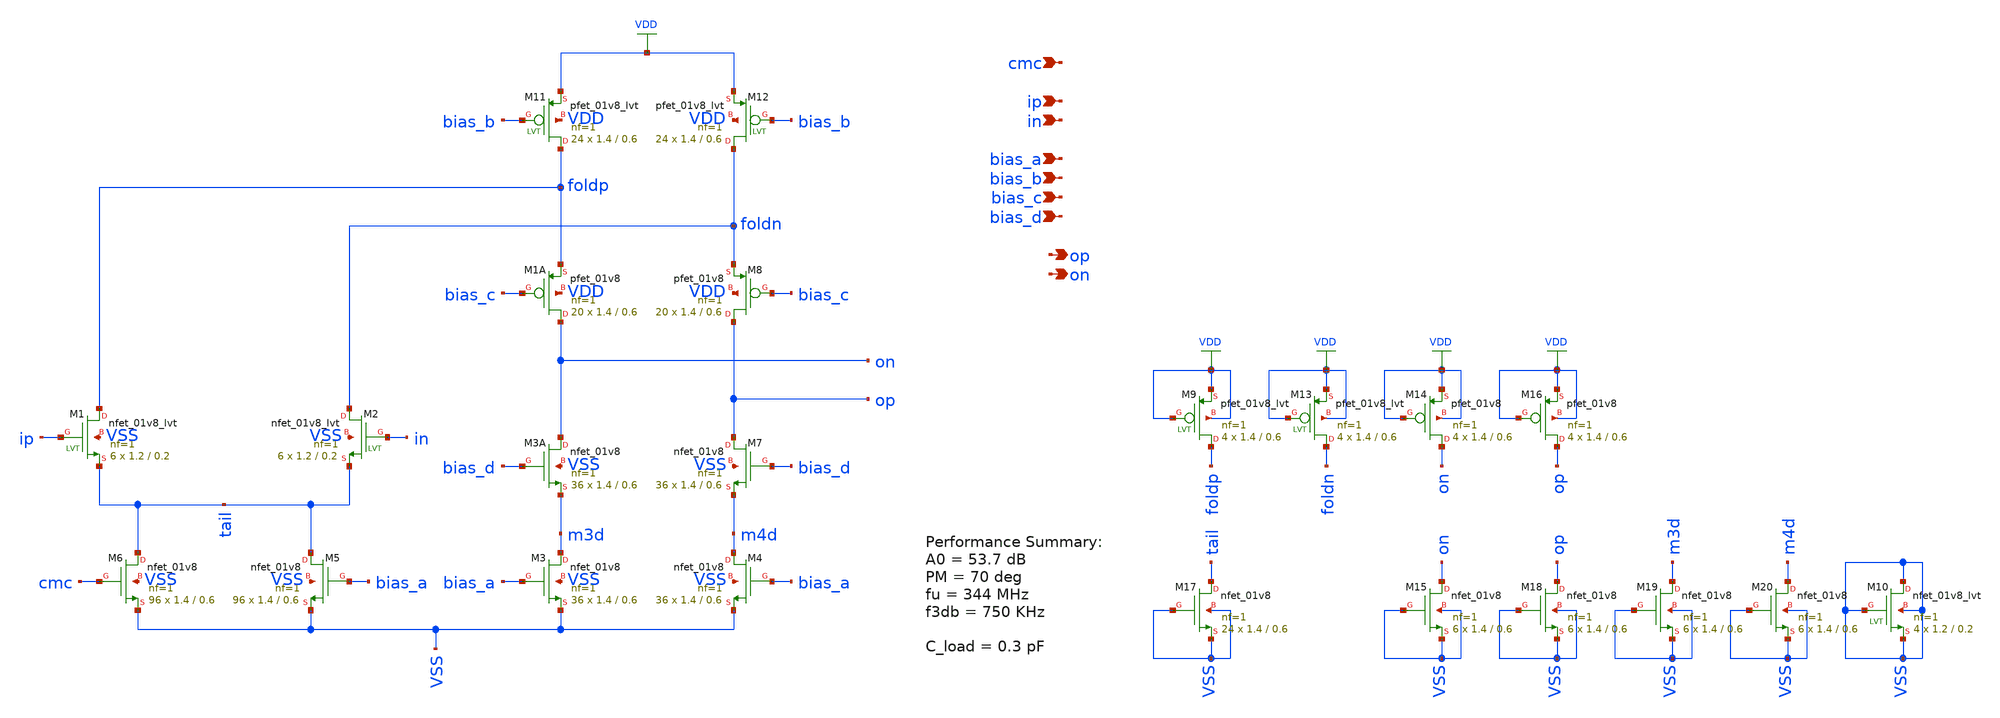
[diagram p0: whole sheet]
** sch_path: design/analog_modulator/schematic/folded_cascode_3_core.sch
**.subckt folded_cascode_3_core cmc ip in bias_a bias_b bias_c bias_d op on
*.ipin cmc
*.ipin ip
*.ipin in
*.ipin bias_a
*.ipin bias_b
*.ipin bias_c
*.ipin bias_d
*.opin op
*.opin on
XM1 foldp ip tail VSS sky130_fd_pr__nfet_01v8_lvt L=0.2 W=1.2 nf=1 ad='int((nf+1)/2) * W/nf * 0.29' as='int((nf+2)/2) * W/nf * 0.29'
+ pd='2*int((nf+1)/2) * (W/nf + 0.29)' ps='2*int((nf+2)/2) * (W/nf + 0.29)' nrd='0.29 / W' nrs='0.29 / W'
+ sa=0 sb=0 sd=0 mult=6 m=6
XM2 foldn in tail VSS sky130_fd_pr__nfet_01v8_lvt L=0.2 W=1.2 nf=1 ad='int((nf+1)/2) * W/nf * 0.29' as='int((nf+2)/2) * W/nf * 0.29'
+ pd='2*int((nf+1)/2) * (W/nf + 0.29)' ps='2*int((nf+2)/2) * (W/nf + 0.29)' nrd='0.29 / W' nrs='0.29 / W'
+ sa=0 sb=0 sd=0 mult=6 m=6
XM6 tail cmc VSS VSS sky130_fd_pr__nfet_01v8 L=0.6 W=1.4 nf=1 ad='int((nf+1)/2) * W/nf * 0.29' as='int((nf+2)/2) * W/nf * 0.29'
+ pd='2*int((nf+1)/2) * (W/nf + 0.29)' ps='2*int((nf+2)/2) * (W/nf + 0.29)' nrd='0.29 / W' nrs='0.29 / W'
+ sa=0 sb=0 sd=0 mult=96 m=96
XM5 tail bias_a VSS VSS sky130_fd_pr__nfet_01v8 L=0.6 W=1.4 nf=1 ad='int((nf+1)/2) * W/nf * 0.29' as='int((nf+2)/2) * W/nf * 0.29'
+ pd='2*int((nf+1)/2) * (W/nf + 0.29)' ps='2*int((nf+2)/2) * (W/nf + 0.29)' nrd='0.29 / W' nrs='0.29 / W'
+ sa=0 sb=0 sd=0 mult=96 m=96
XM11 foldp bias_b VDD VDD sky130_fd_pr__pfet_01v8_lvt L=0.6 W=1.4 nf=1 ad='int((nf+1)/2) * W/nf * 0.29'
+ as='int((nf+2)/2) * W/nf * 0.29' pd='2*int((nf+1)/2) * (W/nf + 0.29)' ps='2*int((nf+2)/2) * (W/nf + 0.29)'
+ nrd='0.29 / W' nrs='0.29 / W' sa=0 sb=0 sd=0 mult=24 m=24
XM12 foldn bias_b VDD VDD sky130_fd_pr__pfet_01v8_lvt L=0.6 W=1.4 nf=1 ad='int((nf+1)/2) * W/nf * 0.29'
+ as='int((nf+2)/2) * W/nf * 0.29' pd='2*int((nf+1)/2) * (W/nf + 0.29)' ps='2*int((nf+2)/2) * (W/nf + 0.29)'
+ nrd='0.29 / W' nrs='0.29 / W' sa=0 sb=0 sd=0 mult=24 m=24
XM1A on bias_c foldp VDD sky130_fd_pr__pfet_01v8 L=0.6 W=1.4 nf=1 ad='int((nf+1)/2) * W/nf * 0.29' as='int((nf+2)/2) * W/nf * 0.29'
+ pd='2*int((nf+1)/2) * (W/nf + 0.29)' ps='2*int((nf+2)/2) * (W/nf + 0.29)' nrd='0.29 / W' nrs='0.29 / W'
+ sa=0 sb=0 sd=0 mult=20 m=20
XM8 op bias_c foldn VDD sky130_fd_pr__pfet_01v8 L=0.6 W=1.4 nf=1 ad='int((nf+1)/2) * W/nf * 0.29' as='int((nf+2)/2) * W/nf * 0.29'
+ pd='2*int((nf+1)/2) * (W/nf + 0.29)' ps='2*int((nf+2)/2) * (W/nf + 0.29)' nrd='0.29 / W' nrs='0.29 / W'
+ sa=0 sb=0 sd=0 mult=20 m=20
XM3A on bias_d m3d VSS sky130_fd_pr__nfet_01v8 L=0.6 W=1.4 nf=1 ad='int((nf+1)/2) * W/nf * 0.29' as='int((nf+2)/2) * W/nf * 0.29'
+ pd='2*int((nf+1)/2) * (W/nf + 0.29)' ps='2*int((nf+2)/2) * (W/nf + 0.29)' nrd='0.29 / W' nrs='0.29 / W'
+ sa=0 sb=0 sd=0 mult=36 m=36
XM7 op bias_d m4d VSS sky130_fd_pr__nfet_01v8 L=0.6 W=1.4 nf=1 ad='int((nf+1)/2) * W/nf * 0.29' as='int((nf+2)/2) * W/nf * 0.29'
+ pd='2*int((nf+1)/2) * (W/nf + 0.29)' ps='2*int((nf+2)/2) * (W/nf + 0.29)' nrd='0.29 / W' nrs='0.29 / W'
+ sa=0 sb=0 sd=0 mult=36 m=36
XM3 m3d bias_a VSS VSS sky130_fd_pr__nfet_01v8 L=0.6 W=1.4 nf=1 ad='int((nf+1)/2) * W/nf * 0.29' as='int((nf+2)/2) * W/nf * 0.29'
+ pd='2*int((nf+1)/2) * (W/nf + 0.29)' ps='2*int((nf+2)/2) * (W/nf + 0.29)' nrd='0.29 / W' nrs='0.29 / W'
+ sa=0 sb=0 sd=0 mult=36 m=36
XM4 m4d bias_a VSS VSS sky130_fd_pr__nfet_01v8 L=0.6 W=1.4 nf=1 ad='int((nf+1)/2) * W/nf * 0.29' as='int((nf+2)/2) * W/nf * 0.29'
+ pd='2*int((nf+1)/2) * (W/nf + 0.29)' ps='2*int((nf+2)/2) * (W/nf + 0.29)' nrd='0.29 / W' nrs='0.29 / W'
+ sa=0 sb=0 sd=0 mult=36 m=36
XM17 tail VSS VSS VSS sky130_fd_pr__nfet_01v8 L=0.6 W=1.4 nf=1 ad='int((nf+1)/2) * W/nf * 0.29' as='int((nf+2)/2) * W/nf * 0.29'
+ pd='2*int((nf+1)/2) * (W/nf + 0.29)' ps='2*int((nf+2)/2) * (W/nf + 0.29)' nrd='0.29 / W' nrs='0.29 / W'
+ sa=0 sb=0 sd=0 mult=24 m=24
XM10 VSS VSS VSS VSS sky130_fd_pr__nfet_01v8_lvt L=0.2 W=1.2 nf=1 ad='int((nf+1)/2) * W/nf * 0.29' as='int((nf+2)/2) * W/nf * 0.29'
+ pd='2*int((nf+1)/2) * (W/nf + 0.29)' ps='2*int((nf+2)/2) * (W/nf + 0.29)' nrd='0.29 / W' nrs='0.29 / W'
+ sa=0 sb=0 sd=0 mult=4 m=4
XM9 foldp VDD VDD VDD sky130_fd_pr__pfet_01v8_lvt L=0.6 W=1.4 nf=1 ad='int((nf+1)/2) * W/nf * 0.29' as='int((nf+2)/2) * W/nf * 0.29'
+ pd='2*int((nf+1)/2) * (W/nf + 0.29)' ps='2*int((nf+2)/2) * (W/nf + 0.29)' nrd='0.29 / W' nrs='0.29 / W'
+ sa=0 sb=0 sd=0 mult=4 m=4
XM13 foldn VDD VDD VDD sky130_fd_pr__pfet_01v8_lvt L=0.6 W=1.4 nf=1 ad='int((nf+1)/2) * W/nf * 0.29'
+ as='int((nf+2)/2) * W/nf * 0.29' pd='2*int((nf+1)/2) * (W/nf + 0.29)' ps='2*int((nf+2)/2) * (W/nf + 0.29)'
+ nrd='0.29 / W' nrs='0.29 / W' sa=0 sb=0 sd=0 mult=4 m=4
XM14 on VDD VDD VDD sky130_fd_pr__pfet_01v8 L=0.6 W=1.4 nf=1 ad='int((nf+1)/2) * W/nf * 0.29' as='int((nf+2)/2) * W/nf * 0.29'
+ pd='2*int((nf+1)/2) * (W/nf + 0.29)' ps='2*int((nf+2)/2) * (W/nf + 0.29)' nrd='0.29 / W' nrs='0.29 / W'
+ sa=0 sb=0 sd=0 mult=4 m=4
XM15 on VSS VSS VSS sky130_fd_pr__nfet_01v8 L=0.6 W=1.4 nf=1 ad='int((nf+1)/2) * W/nf * 0.29' as='int((nf+2)/2) * W/nf * 0.29'
+ pd='2*int((nf+1)/2) * (W/nf + 0.29)' ps='2*int((nf+2)/2) * (W/nf + 0.29)' nrd='0.29 / W' nrs='0.29 / W'
+ sa=0 sb=0 sd=0 mult=6 m=6
XM16 op VDD VDD VDD sky130_fd_pr__pfet_01v8 L=0.6 W=1.4 nf=1 ad='int((nf+1)/2) * W/nf * 0.29' as='int((nf+2)/2) * W/nf * 0.29'
+ pd='2*int((nf+1)/2) * (W/nf + 0.29)' ps='2*int((nf+2)/2) * (W/nf + 0.29)' nrd='0.29 / W' nrs='0.29 / W'
+ sa=0 sb=0 sd=0 mult=4 m=4
XM18 op VSS VSS VSS sky130_fd_pr__nfet_01v8 L=0.6 W=1.4 nf=1 ad='int((nf+1)/2) * W/nf * 0.29' as='int((nf+2)/2) * W/nf * 0.29'
+ pd='2*int((nf+1)/2) * (W/nf + 0.29)' ps='2*int((nf+2)/2) * (W/nf + 0.29)' nrd='0.29 / W' nrs='0.29 / W'
+ sa=0 sb=0 sd=0 mult=6 m=6
XM19 m3d VSS VSS VSS sky130_fd_pr__nfet_01v8 L=0.6 W=1.4 nf=1 ad='int((nf+1)/2) * W/nf * 0.29' as='int((nf+2)/2) * W/nf * 0.29'
+ pd='2*int((nf+1)/2) * (W/nf + 0.29)' ps='2*int((nf+2)/2) * (W/nf + 0.29)' nrd='0.29 / W' nrs='0.29 / W'
+ sa=0 sb=0 sd=0 mult=6 m=6
XM20 m4d VSS VSS VSS sky130_fd_pr__nfet_01v8 L=0.6 W=1.4 nf=1 ad='int((nf+1)/2) * W/nf * 0.29' as='int((nf+2)/2) * W/nf * 0.29'
+ pd='2*int((nf+1)/2) * (W/nf + 0.29)' ps='2*int((nf+2)/2) * (W/nf + 0.29)' nrd='0.29 / W' nrs='0.29 / W'
+ sa=0 sb=0 sd=0 mult=6 m=6
**.ends
.GLOBAL VDD
.end
